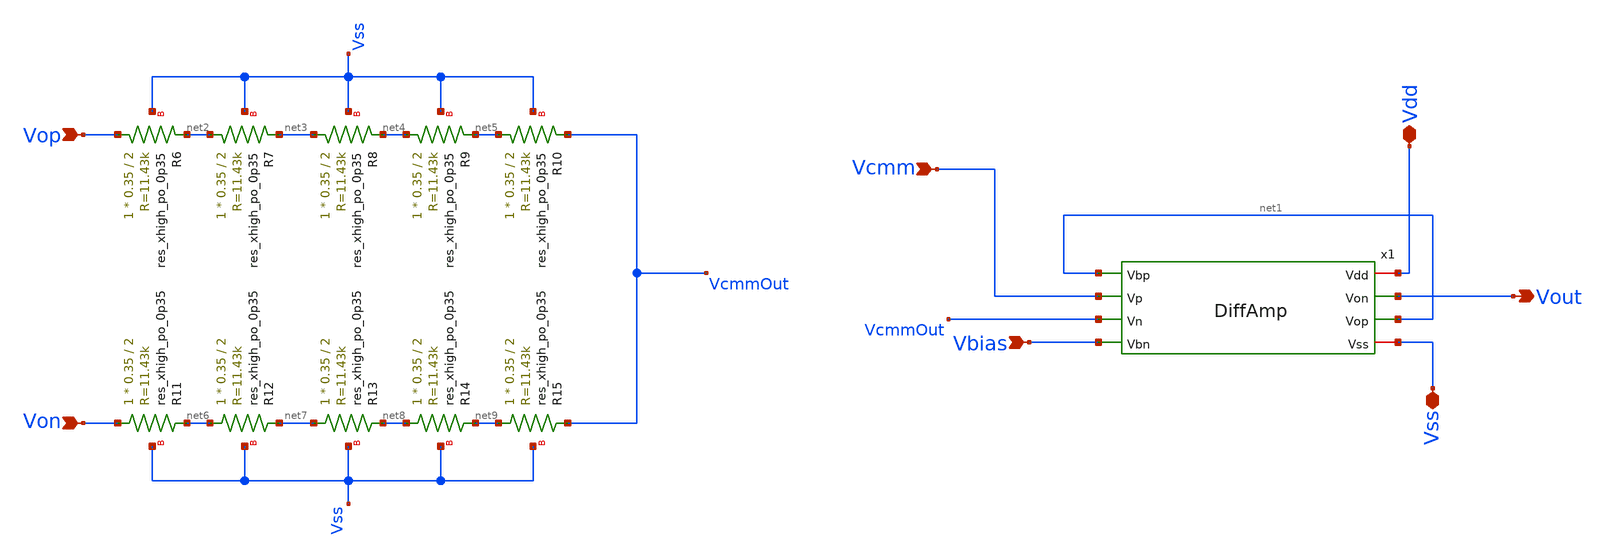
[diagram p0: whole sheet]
** sch_path: Circuits/Examples/MillerOpAmpCMMFB/CMMFeedback.sch
**.subckt CMMFeedback Vbias Vout Vop Vcmm Von Vss Vdd
*.ipin Vbias
*.opin Vout
*.ipin Vop
*.ipin Vcmm
*.ipin Von
*.iopin Vss
*.iopin Vdd
XR6 Vop net2 Vss sky130_fd_pr__res_xhigh_po_0p35 L=2 mult=1 m=1
XR7 net2 net3 Vss sky130_fd_pr__res_xhigh_po_0p35 L=2 mult=1 m=1
XR8 net3 net4 Vss sky130_fd_pr__res_xhigh_po_0p35 L=2 mult=1 m=1
XR9 net4 net5 Vss sky130_fd_pr__res_xhigh_po_0p35 L=2 mult=1 m=1
XR10 net5 VcmmOut Vss sky130_fd_pr__res_xhigh_po_0p35 L=2 mult=1 m=1
XR11 Von net6 Vss sky130_fd_pr__res_xhigh_po_0p35 L=2 mult=1 m=1
XR12 net6 net7 Vss sky130_fd_pr__res_xhigh_po_0p35 L=2 mult=1 m=1
XR13 net7 net8 Vss sky130_fd_pr__res_xhigh_po_0p35 L=2 mult=1 m=1
XR14 net8 net9 Vss sky130_fd_pr__res_xhigh_po_0p35 L=2 mult=1 m=1
XR15 net9 VcmmOut Vss sky130_fd_pr__res_xhigh_po_0p35 L=2 mult=1 m=1
x1 Vdd net1 Vout net1 Vcmm VcmmOut Vbias Vss DiffAmp
**.ends

* expanding   symbol:
*+  /home/jakob/Documents/AutomatedLayoutGeneration/Circuits/MillerOpAmpCMMFB/DiffAmp.sym # of pins=8
** sym_path: Circuits/Examples/OpAmp/DiffAmp.sym
** sch_path: Circuits/Examples/OpAmp/DiffAmp.sch
.subckt DiffAmp Vdd Vbp Von Vop Vp Vn Vbn Vss
*.iopin Vdd
*.iopin Vss
*.ipin Vp
*.ipin Vn
*.ipin Vbn
*.ipin Vbp
*.opin Vop
*.opin Von
XM1 Vop Vp vmid Vss sky130_fd_pr__nfet_01v8 L=1 W=1 nf=1 ad='int((nf+1)/2) * W/nf * 0.29' as='int((nf+2)/2) * W/nf * 0.29'
+ pd='2*int((nf+1)/2) * (W/nf + 0.29)' ps='2*int((nf+2)/2) * (W/nf + 0.29)' nrd='0.29 / W' nrs='0.29 / W'
+ sa=0 sb=0 sd=0 mult=1 m=1
XM2 Von Vn vmid Vss sky130_fd_pr__nfet_01v8 L=1 W=1 nf=1 ad='int((nf+1)/2) * W/nf * 0.29' as='int((nf+2)/2) * W/nf * 0.29'
+ pd='2*int((nf+1)/2) * (W/nf + 0.29)' ps='2*int((nf+2)/2) * (W/nf + 0.29)' nrd='0.29 / W' nrs='0.29 / W'
+ sa=0 sb=0 sd=0 mult=1 m=1
XM3 Vop Vbp Vdd Vdd sky130_fd_pr__pfet_01v8 L=1 W=2 nf=1 ad='int((nf+1)/2) * W/nf * 0.29' as='int((nf+2)/2) * W/nf * 0.29'
+ pd='2*int((nf+1)/2) * (W/nf + 0.29)' ps='2*int((nf+2)/2) * (W/nf + 0.29)' nrd='0.29 / W' nrs='0.29 / W'
+ sa=0 sb=0 sd=0 mult=1 m=1
XM4 Von Vbp Vdd Vdd sky130_fd_pr__pfet_01v8 L=1 W=2 nf=1 ad='int((nf+1)/2) * W/nf * 0.29' as='int((nf+2)/2) * W/nf * 0.29'
+ pd='2*int((nf+1)/2) * (W/nf + 0.29)' ps='2*int((nf+2)/2) * (W/nf + 0.29)' nrd='0.29 / W' nrs='0.29 / W'
+ sa=0 sb=0 sd=0 mult=1 m=1
XM5 vmid Vbn Vss Vss sky130_fd_pr__nfet_01v8 L=2 W=1 nf=1 ad='int((nf+1)/2) * W/nf * 0.29' as='int((nf+2)/2) * W/nf * 0.29'
+ pd='2*int((nf+1)/2) * (W/nf + 0.29)' ps='2*int((nf+2)/2) * (W/nf + 0.29)' nrd='0.29 / W' nrs='0.29 / W'
+ sa=0 sb=0 sd=0 mult=1 m=1
.ends

.end
